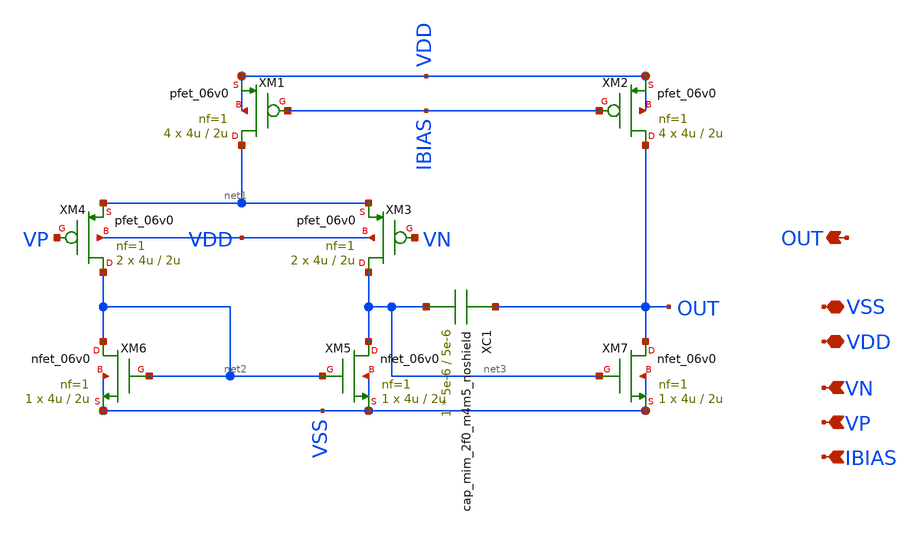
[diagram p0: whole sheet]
** sch_path: designs/libs/core_p-ota/p-6v-ota/p-ota.sch
**.subckt p-ota VN VP OUT VDD VSS IBIAS
*.ipin VN
*.ipin VP
*.opin OUT
*.iopin VDD
*.iopin VSS
*.ipin IBIAS
XM3 net3 VN net1 VDD pfet_06v0 L=2u W=4u nf=1 ad='int((nf+1)/2) * W/nf * 0.18u' as='int((nf+2)/2) * W/nf * 0.18u'
+ pd='2*int((nf+1)/2) * (W/nf + 0.18u)' ps='2*int((nf+2)/2) * (W/nf + 0.18u)' nrd='0.18u / W' nrs='0.18u / W'
+ sa=0 sb=0 sd=0 m=2
XM4 net2 VP net1 VDD pfet_06v0 L=2u W=4u nf=1 ad='int((nf+1)/2) * W/nf * 0.18u' as='int((nf+2)/2) * W/nf * 0.18u'
+ pd='2*int((nf+1)/2) * (W/nf + 0.18u)' ps='2*int((nf+2)/2) * (W/nf + 0.18u)' nrd='0.18u / W' nrs='0.18u / W'
+ sa=0 sb=0 sd=0 m=2
XM5 net3 net2 VSS VSS nfet_06v0 L=2u W=4u nf=1 ad='int((nf+1)/2) * W/nf * 0.18u' as='int((nf+2)/2) * W/nf * 0.18u'
+ pd='2*int((nf+1)/2) * (W/nf + 0.18u)' ps='2*int((nf+2)/2) * (W/nf + 0.18u)' nrd='0.18u / W' nrs='0.18u / W'
+ sa=0 sb=0 sd=0 m=1
XM6 net2 net2 VSS VSS nfet_06v0 L=2u W=4u nf=1 ad='int((nf+1)/2) * W/nf * 0.18u' as='int((nf+2)/2) * W/nf * 0.18u'
+ pd='2*int((nf+1)/2) * (W/nf + 0.18u)' ps='2*int((nf+2)/2) * (W/nf + 0.18u)' nrd='0.18u / W' nrs='0.18u / W'
+ sa=0 sb=0 sd=0 m=1
XM1 net1 IBIAS VDD VDD pfet_06v0 L=2u W=4u nf=1 ad='int((nf+1)/2) * W/nf * 0.18u' as='int((nf+2)/2) * W/nf * 0.18u'
+ pd='2*int((nf+1)/2) * (W/nf + 0.18u)' ps='2*int((nf+2)/2) * (W/nf + 0.18u)' nrd='0.18u / W' nrs='0.18u / W'
+ sa=0 sb=0 sd=0 m=4
XM2 OUT IBIAS VDD VDD pfet_06v0 L=2u W=4u nf=1 ad='int((nf+1)/2) * W/nf * 0.18u' as='int((nf+2)/2) * W/nf * 0.18u'
+ pd='2*int((nf+1)/2) * (W/nf + 0.18u)' ps='2*int((nf+2)/2) * (W/nf + 0.18u)' nrd='0.18u / W' nrs='0.18u / W'
+ sa=0 sb=0 sd=0 m=4
XM7 OUT net3 VSS VSS nfet_06v0 L=2u W=4u nf=1 ad='int((nf+1)/2) * W/nf * 0.18u' as='int((nf+2)/2) * W/nf * 0.18u'
+ pd='2*int((nf+1)/2) * (W/nf + 0.18u)' ps='2*int((nf+2)/2) * (W/nf + 0.18u)' nrd='0.18u / W' nrs='0.18u / W'
+ sa=0 sb=0 sd=0 m=1
XC1 OUT net3 cap_mim_2f0_m4m5_noshield c_width=5e-6 c_length=5e-6 m=1
**.ends
.end
